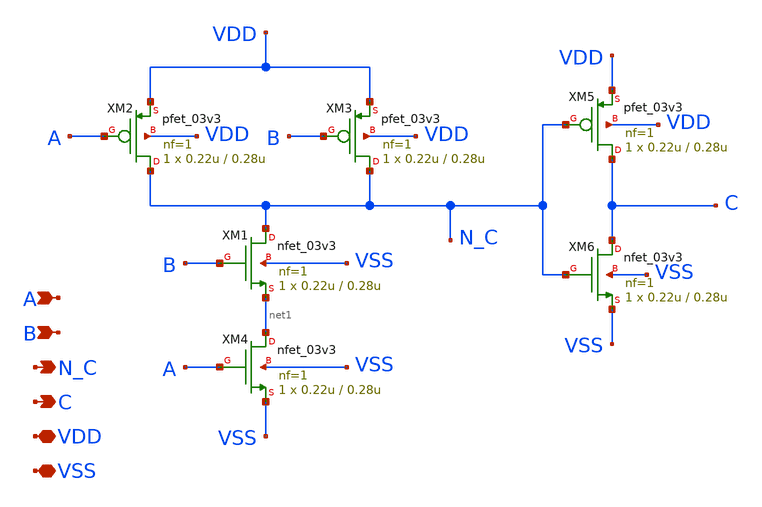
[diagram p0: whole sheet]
** sch_path: schematics/logic-gates/and/and.sch
**.subckt and A B C N_C VDD VSS
*.ipin A
*.ipin B
*.opin C
*.opin N_C
*.iopin VDD
*.iopin VSS
XM1 N_C B net1 VSS nfet_03v3 L=0.28u W=0.22u nf=1 ad='int((nf+1)/2) * W/nf * 0.18u' as='int((nf+2)/2) * W/nf * 0.18u'
+ pd='2*int((nf+1)/2) * (W/nf + 0.18u)' ps='2*int((nf+2)/2) * (W/nf + 0.18u)' nrd='0.18u / W' nrs='0.18u / W'
+ sa=0 sb=0 sd=0 m=1
XM2 N_C A VDD VDD pfet_03v3 L=0.28u W=0.22u nf=1 ad='int((nf+1)/2) * W/nf * 0.18u' as='int((nf+2)/2) * W/nf * 0.18u'
+ pd='2*int((nf+1)/2) * (W/nf + 0.18u)' ps='2*int((nf+2)/2) * (W/nf + 0.18u)' nrd='0.18u / W' nrs='0.18u / W'
+ sa=0 sb=0 sd=0 m=1
XM3 N_C B VDD VDD pfet_03v3 L=0.28u W=0.22u nf=1 ad='int((nf+1)/2) * W/nf * 0.18u' as='int((nf+2)/2) * W/nf * 0.18u'
+ pd='2*int((nf+1)/2) * (W/nf + 0.18u)' ps='2*int((nf+2)/2) * (W/nf + 0.18u)' nrd='0.18u / W' nrs='0.18u / W'
+ sa=0 sb=0 sd=0 m=1
XM4 net1 A VSS VSS nfet_03v3 L=0.28u W=0.22u nf=1 ad='int((nf+1)/2) * W/nf * 0.18u' as='int((nf+2)/2) * W/nf * 0.18u'
+ pd='2*int((nf+1)/2) * (W/nf + 0.18u)' ps='2*int((nf+2)/2) * (W/nf + 0.18u)' nrd='0.18u / W' nrs='0.18u / W'
+ sa=0 sb=0 sd=0 m=1
XM5 C N_C VDD VDD pfet_03v3 L=0.28u W=0.22u nf=1 ad='int((nf+1)/2) * W/nf * 0.18u' as='int((nf+2)/2) * W/nf * 0.18u'
+ pd='2*int((nf+1)/2) * (W/nf + 0.18u)' ps='2*int((nf+2)/2) * (W/nf + 0.18u)' nrd='0.18u / W' nrs='0.18u / W'
+ sa=0 sb=0 sd=0 m=1
XM6 C N_C VSS VSS nfet_03v3 L=0.28u W=0.22u nf=1 ad='int((nf+1)/2) * W/nf * 0.18u' as='int((nf+2)/2) * W/nf * 0.18u'
+ pd='2*int((nf+1)/2) * (W/nf + 0.18u)' ps='2*int((nf+2)/2) * (W/nf + 0.18u)' nrd='0.18u / W' nrs='0.18u / W'
+ sa=0 sb=0 sd=0 m=1
**.ends
.end
